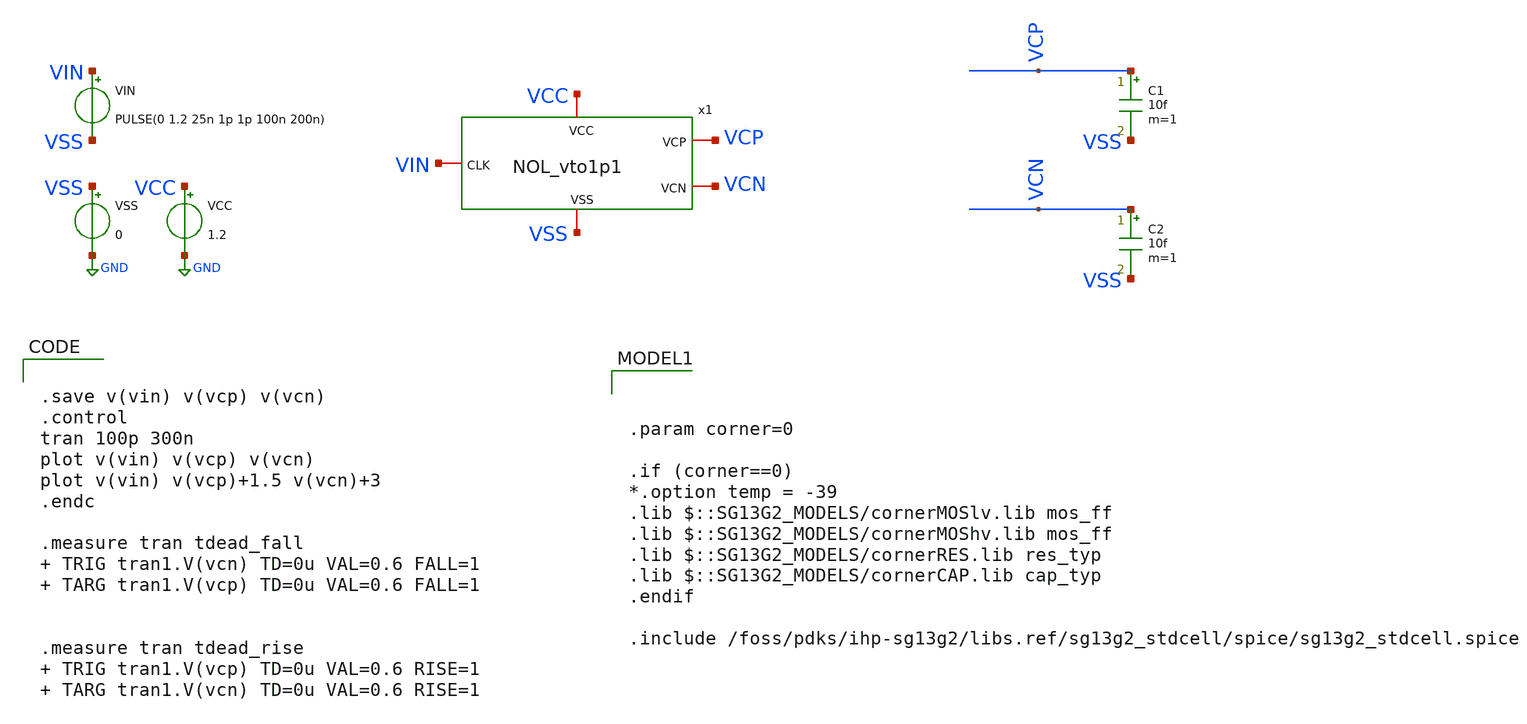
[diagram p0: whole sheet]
** sch_path: xschem/IHP_digital/NOL/tb_NOL_vto1p1.sch
**.subckt tb_NOL_vto1p1
VCC VCC GND 1.2
VSS VSS GND 0
VIN VIN VSS PULSE(0 1.2 25n 1p 1p 100n 200n)
C1 VCP VSS 10f m=1
C2 VCN VSS 10f m=1
x1 VCC VSS VCP VIN VCN NOL_vto1p1
**** begin user architecture code


.save v(vin) v(vcp) v(vcn)
.control
tran 100p 300n
plot v(vin) v(vcp) v(vcn)
plot v(vin) v(vcp)+1.5 v(vcn)+3
.endc

.measure tran tdead_fall  TRIG tran1.V(vcn) TD=0u VAL=0.6 FALL=1  TARG tran1.V(vcp) TD=0u VAL=0.6
+ FALL=1


.measure tran tdead_rise  TRIG tran1.V(vcp) TD=0u VAL=0.6 RISE=1  TARG tran1.V(vcn) TD=0u VAL=0.6
+ RISE=1






.param corner=0

.if (corner==0)
*.option temp = -39
.lib $::SG13G2_MODELS/cornerMOSlv.lib mos_ff
.lib $::SG13G2_MODELS/cornerMOShv.lib mos_ff
.lib $::SG13G2_MODELS/cornerRES.lib res_typ
.lib $::SG13G2_MODELS/cornerCAP.lib cap_typ
.endif

.include /foss/pdks/ihp-sg13g2/libs.ref/sg13g2_stdcell/spice/sg13g2_stdcell.spice

**** end user architecture code
**.ends

* expanding   symbol:
*+  /foss/designs/SSCS-Chipathon-2025_AC3E-Chile-team/xschem/IHP_digital/NOL/NOL_vto1p1.sym # of pins=5
** sym_path: xschem/gf180_digital/NOL/NOL_vto1p1.sym
** sch_path: xschem/gf180_digital/NOL/NOL_vto1p1.sch
.subckt NOL_vto1p1 VDDd VSSd VCP CLK VCN
*.iopin CLK
*.iopin VCP
*.iopin VCN
*.iopin VDDd
*.iopin VSSd
x11 B1 VSSd VDDd VSSd VDDd net1 gf180mcu_fd_sc_mcu9t5v0__inv_1
x12 net1 VSSd VDDd VSSd VDDd net3 gf180mcu_fd_sc_mcu9t5v0__inv_2
x13 net3 VSSd VDDd VSSd VDDd VCP gf180mcu_fd_sc_mcu9t5v0__inv_4
x14 A1 B1 VSSd VDDd VSSd VDDd C1 gf180mcu_fd_sc_mcu9t5v0__nor2_1
x15 VDDd VSSd C1 B2 large_delay_vto1p1
x4 VDDd VSSd C2 B1 large_delay_vto1p1
x1 B2 CLK VSSd VDDd VSSd VDDd C2 gf180mcu_fd_sc_mcu9t5v0__nor2_1
x3 CLK VSSd VDDd VSSd VDDd A1 gf180mcu_fd_sc_mcu9t5v0__inv_1
x5 B2 VSSd VDDd VSSd VDDd net2 gf180mcu_fd_sc_mcu9t5v0__inv_1
x6 net2 VSSd VDDd VSSd VDDd VCN gf180mcu_fd_sc_mcu9t5v0__inv_4
.ends


* expanding   symbol:  gf180_digital/large_delay/large_delay_vto1p1.sym # of pins=4
** sym_path: xschem/gf180_digital/large_delay/large_delay_vto1p1.sym
** sch_path: xschem/gf180_digital/large_delay/large_delay_vto1p1.sch
.subckt large_delay_vto1p1 VDDd VSSd VIN VOUT
*.iopin VIN
*.iopin VOUT
*.iopin VDDd
*.iopin VSSd
x1 VIN VOUT VDDd VDDd VSSd VSSd gf180mcu_fd_sc_mcu9t5v0__dlyd_1
.ends

.GLOBAL GND
.end
